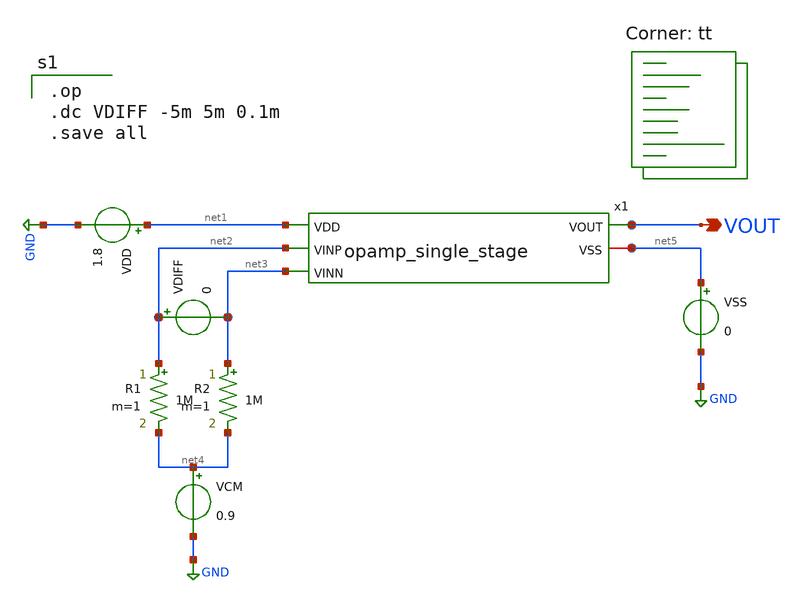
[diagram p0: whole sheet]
** sch_path: schematics/tb_dc_analysis.sch
**.subckt tb_dc_analysis VOUT
*.opin VOUT
VDD net1 GND 1.8
VDIFF net2 net3 0
R1 net2 net4 1M m=1
R2 net3 net4 1M m=1
VCM net4 GND 0.9
VSS net5 GND 0
x1 net1 VOUT net2 net3 net5 opamp_single_stage
**** begin user architecture code

.op
.dc VDIFF -5m 5m 0.1m
.save all


.lib $::SKYWATER_MODELS/sky130.lib.spice tt
**** end user architecture code
**.ends
.GLOBAL GND
.end
